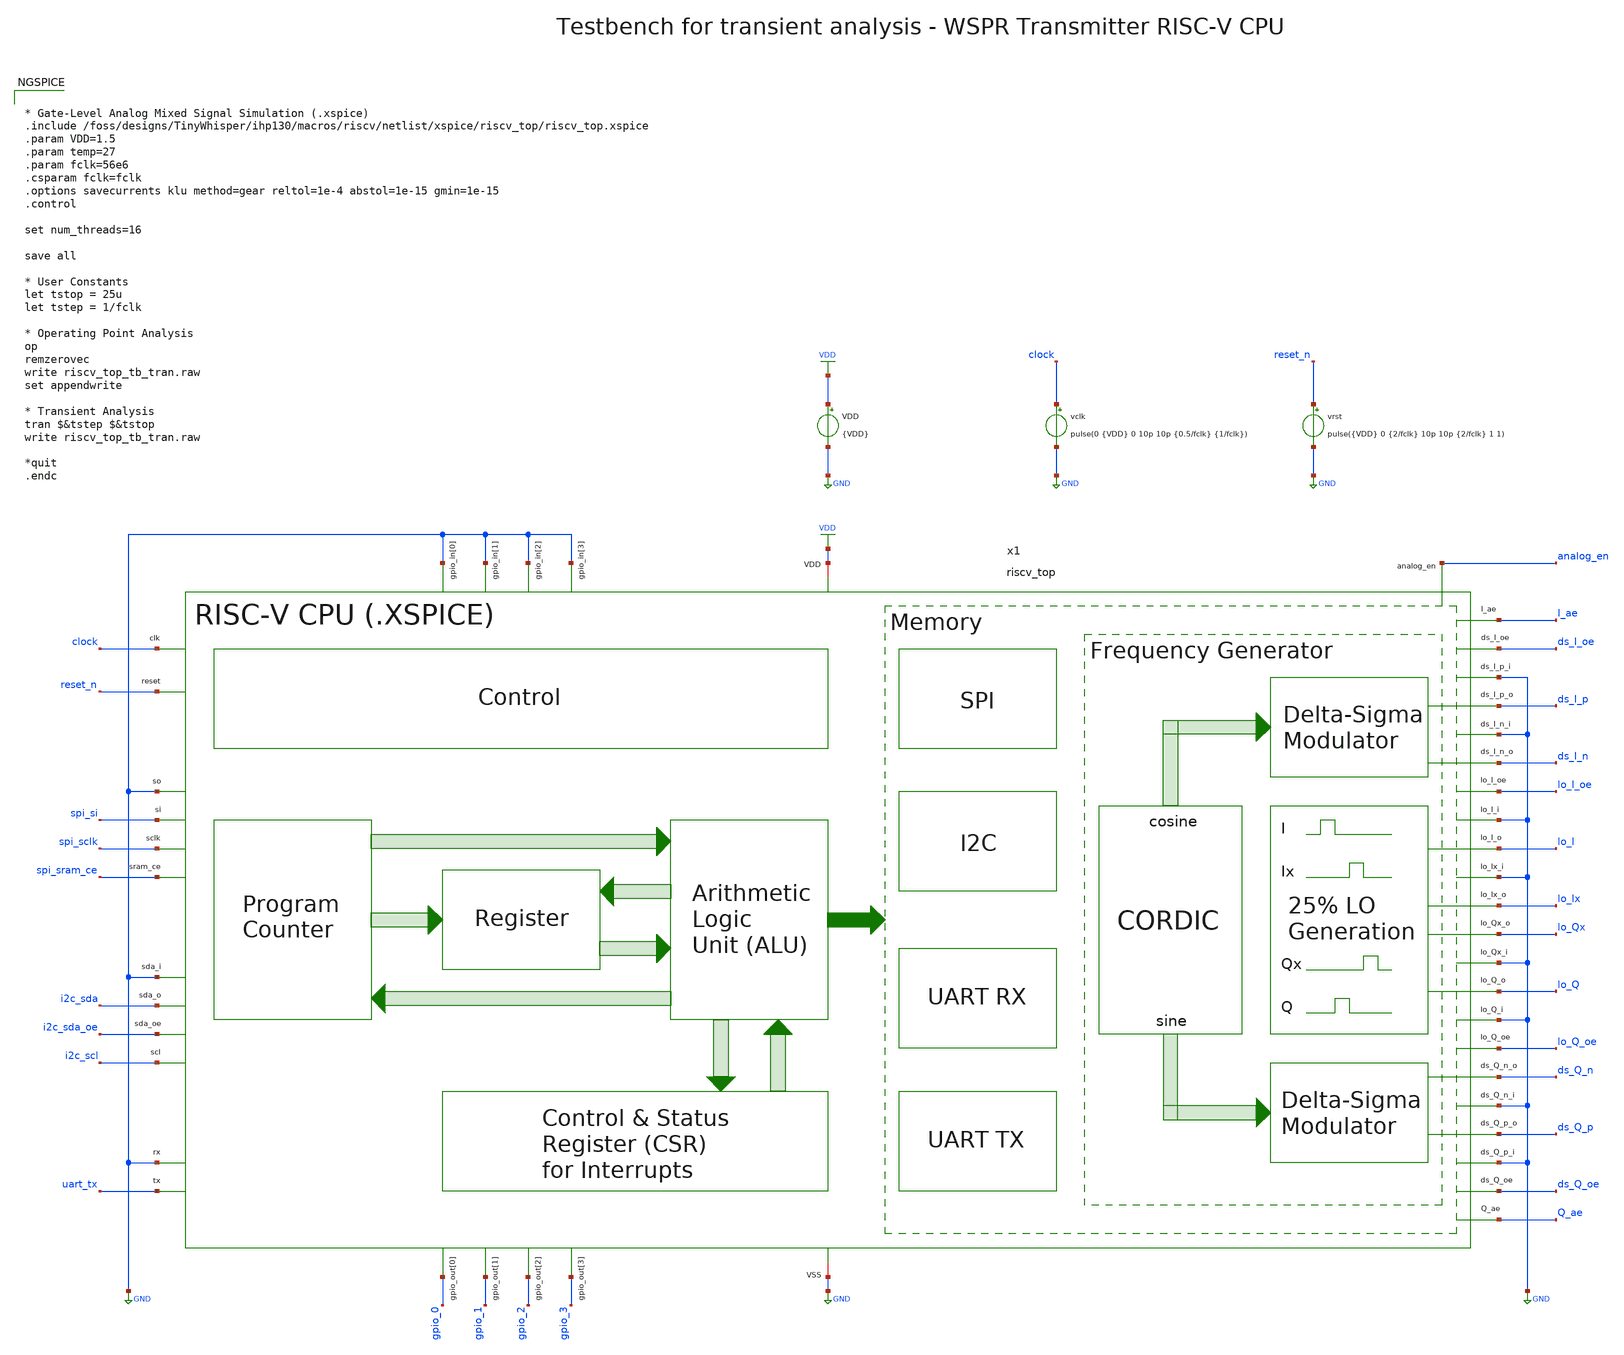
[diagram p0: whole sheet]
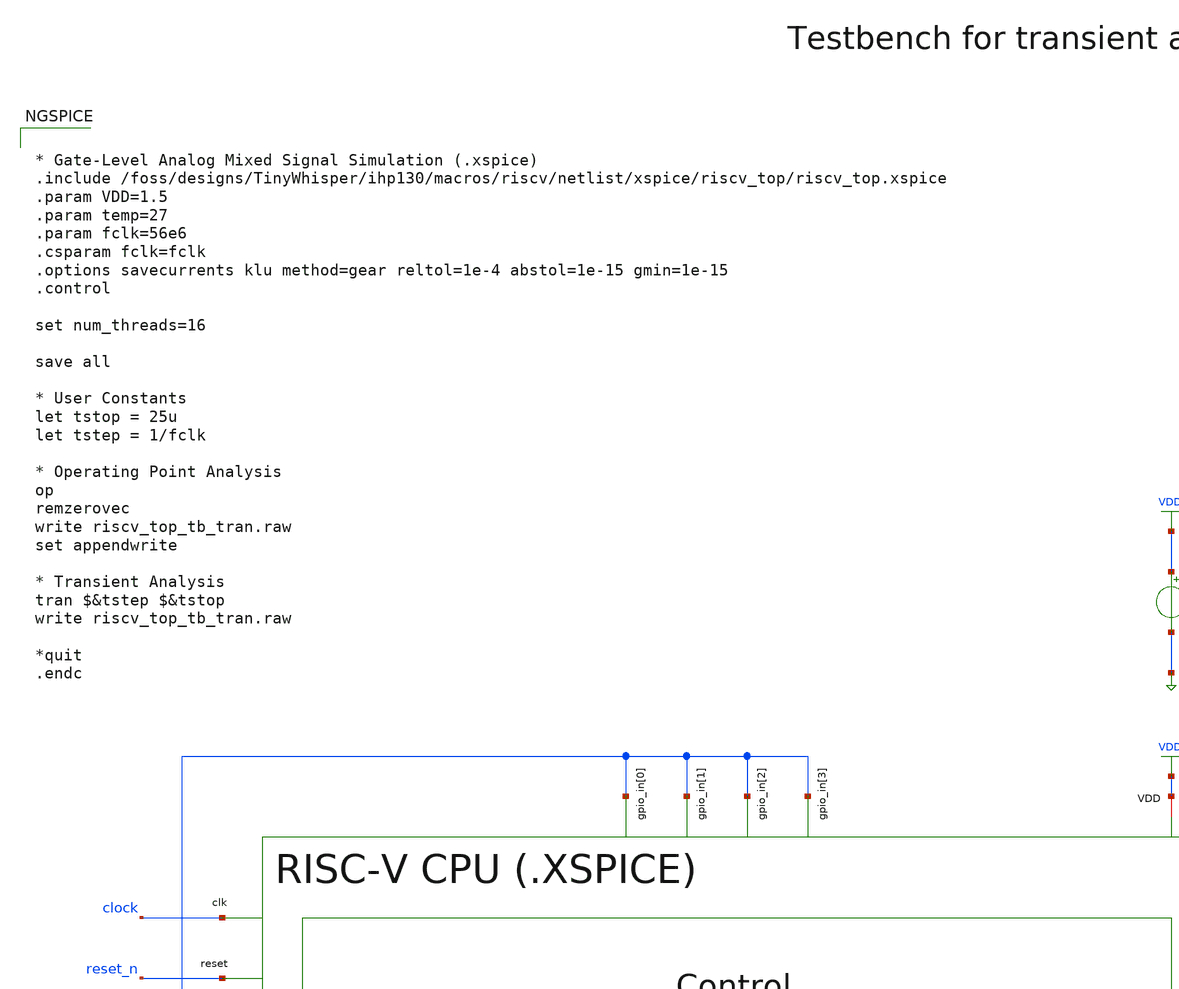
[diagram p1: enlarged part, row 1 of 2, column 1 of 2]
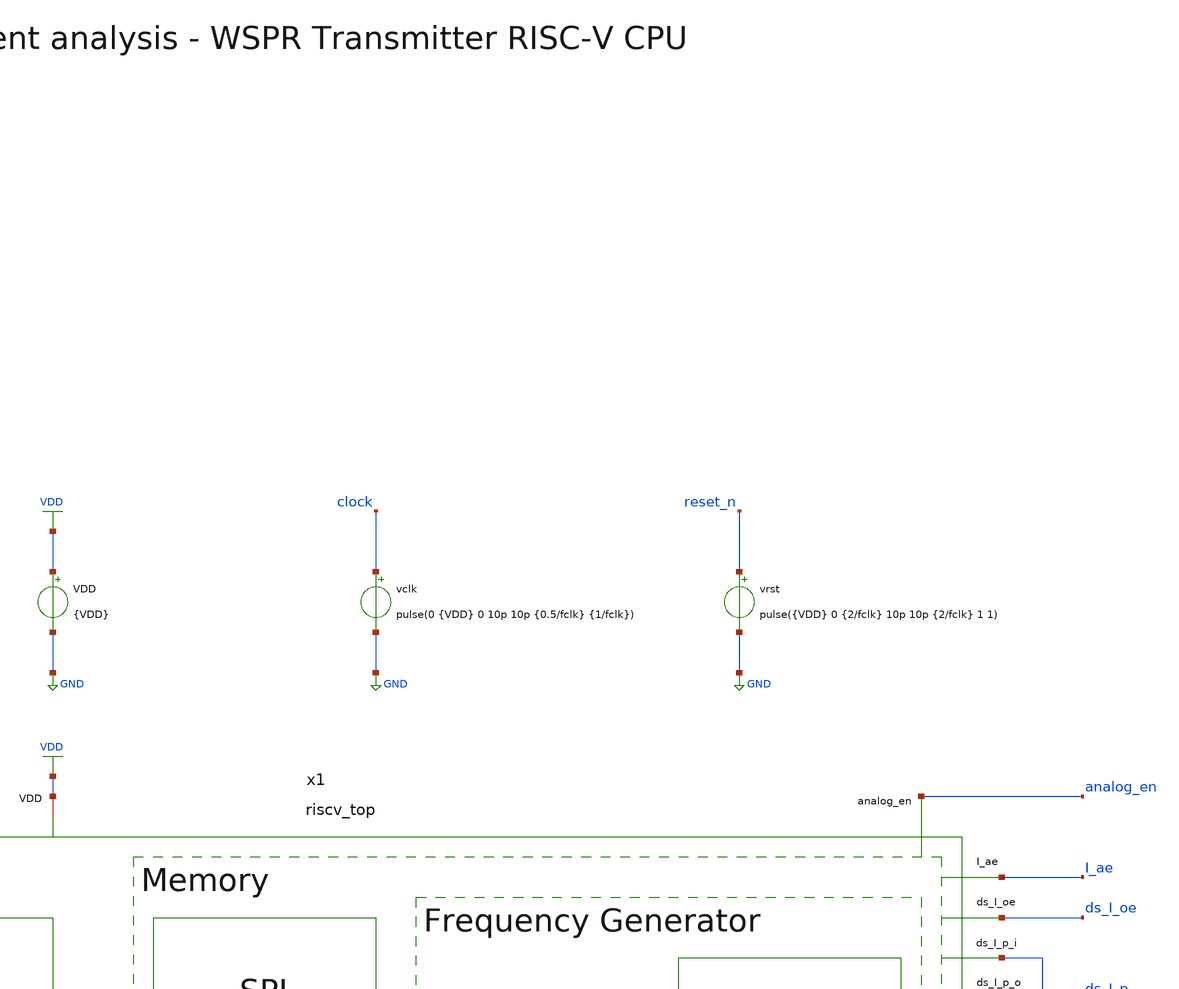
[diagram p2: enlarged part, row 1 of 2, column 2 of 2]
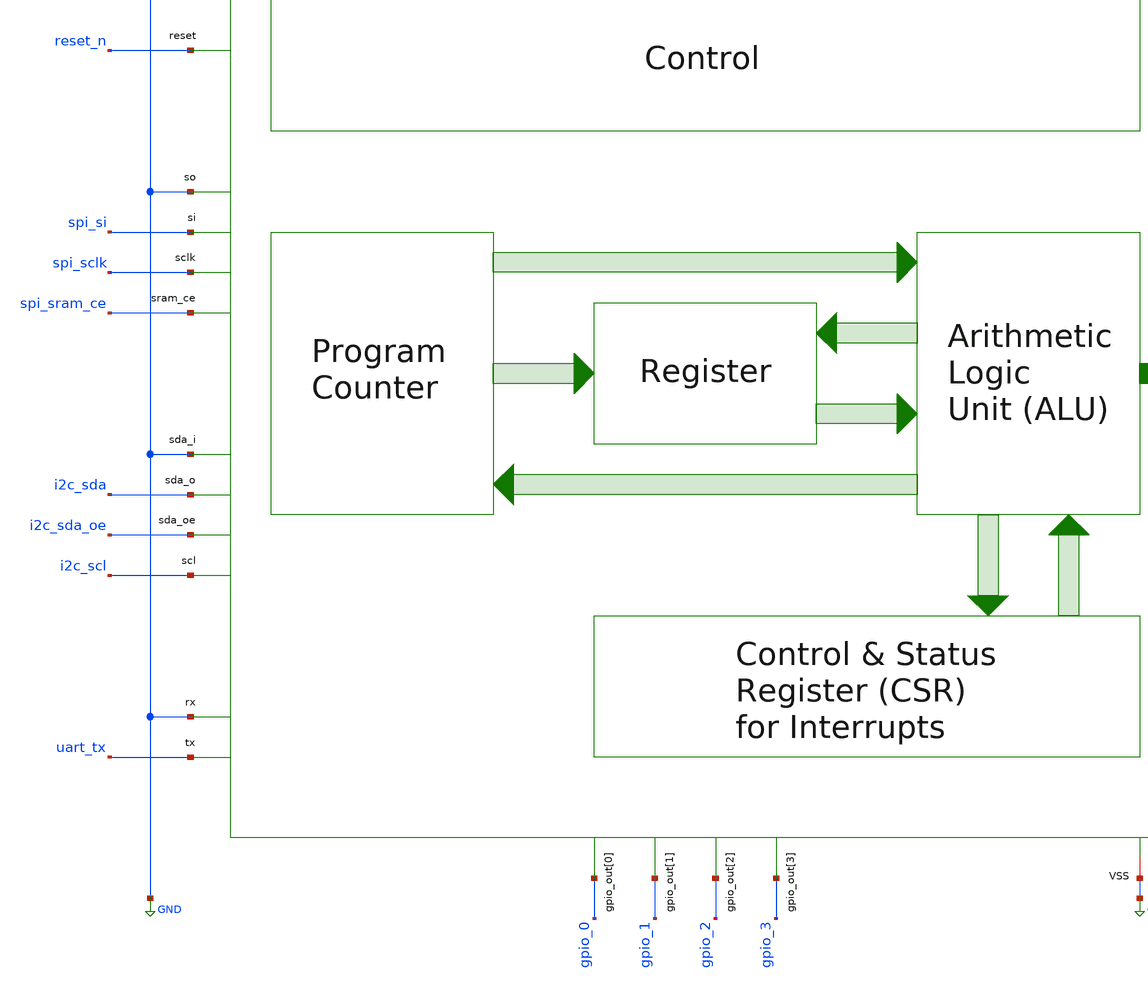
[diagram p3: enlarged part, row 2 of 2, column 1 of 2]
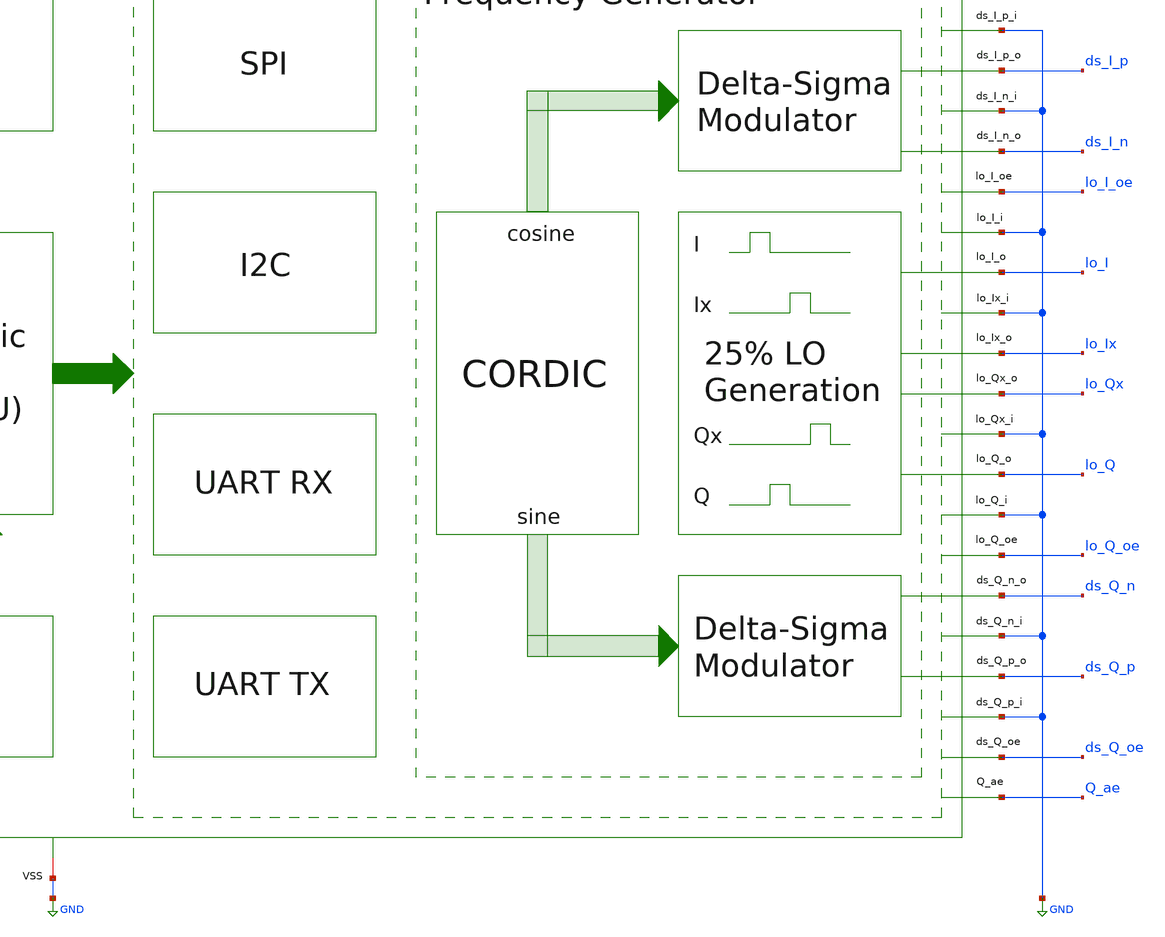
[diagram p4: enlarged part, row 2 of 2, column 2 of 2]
** sch_path: ihp130/macros/riscv/testbenches/xschem/riscv_top_tb_tran.sch
**.subckt riscv_top_tb_tran
VDD VDD GND {VDD}
vclk clock GND pulse(0 {VDD} 0 10p 10p {0.5/fclk} {1/fclk})
vrst reset_n GND pulse({VDD} 0 {2/fclk} 10p 10p {2/fclk} 1 1)
x1 VDD GND I_ae Q_ae clock GND ds_I_n ds_I_oe GND ds_I_p GND ds_Q_n ds_Q_oe GND ds_Q_p GND lo_I
+ lo_I_oe GND lo_Ix GND lo_Q lo_Q_oe GND lo_Qx reset_n GND i2c_scl spi_sclk GND i2c_sda i2c_sda_oe spi_si GND
+ spi_sram_ce uart_tx GND GND GND GND gpio_0 gpio_1 gpio_2 gpio_3 analog_en riscv_top
**** begin user architecture code


* Gate-Level Analog Mixed Signal Simulation (.xspice)
.include /foss/designs/TinyWhisper/ihp130/macros/riscv/netlist/xspice/riscv_top/riscv_top.xspice
.param VDD=1.5
.param temp=27
.param fclk=56e6
.csparam fclk=fclk
.options savecurrents klu method=gear reltol=1e-4 abstol=1e-15 gmin=1e-15
.control

set num_threads=16

save all

* User Constants
let tstop = 25u
let tstep = 1/fclk

* Operating Point Analysis
op
remzerovec
write riscv_top_tb_tran.raw
set appendwrite

* Transient Analysis
tran $&tstep $&tstop
write riscv_top_tb_tran.raw

*quit
.endc



.lib cornerMOSlv.lib mos_tt
.lib cornerMOShv.lib mos_tt
.lib cornerHBT.lib hbt_typ
.lib cornerRES.lib res_typ
.lib cornerCAP.lib cap_typ
.lib cornerDIO.lib dio_tt

**** end user architecture code
**.ends
.GLOBAL GND
.GLOBAL VDD
.end
